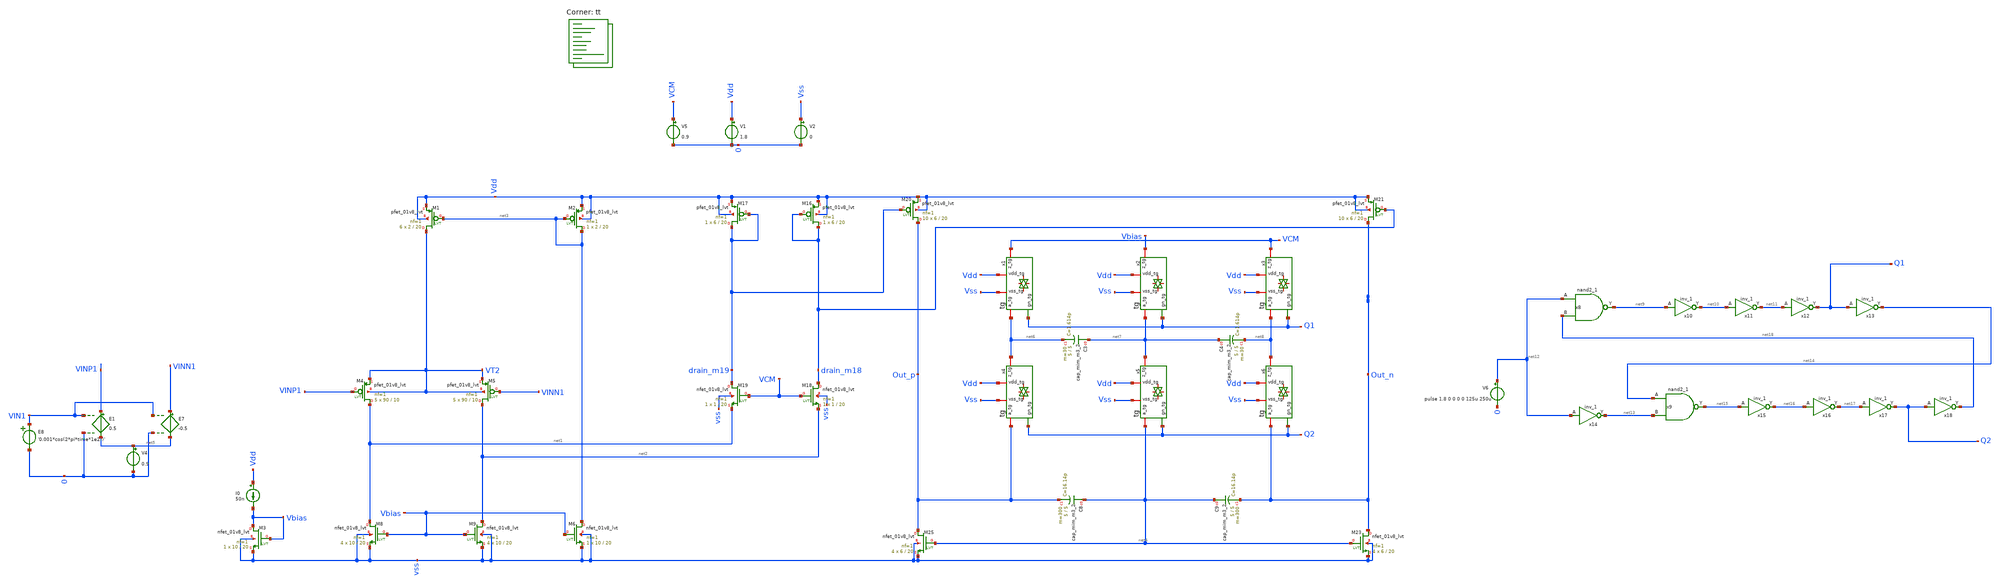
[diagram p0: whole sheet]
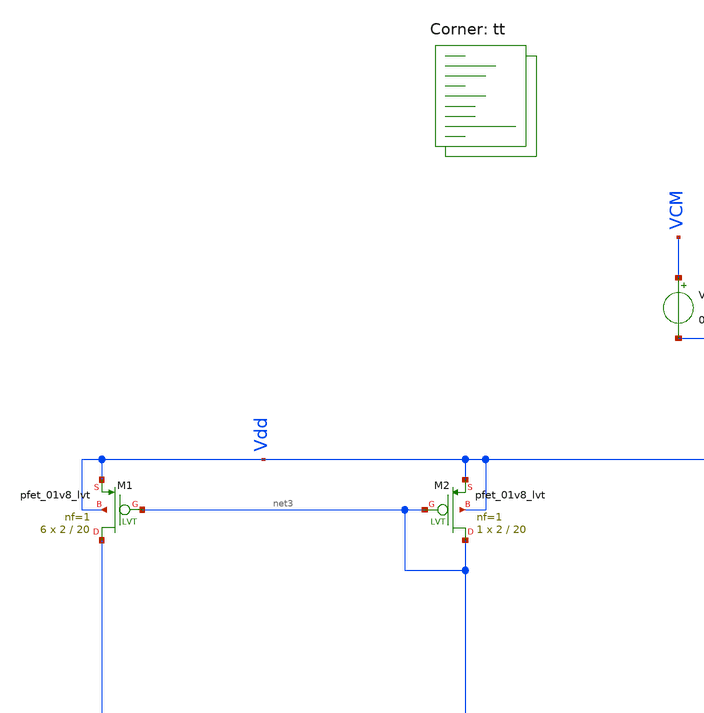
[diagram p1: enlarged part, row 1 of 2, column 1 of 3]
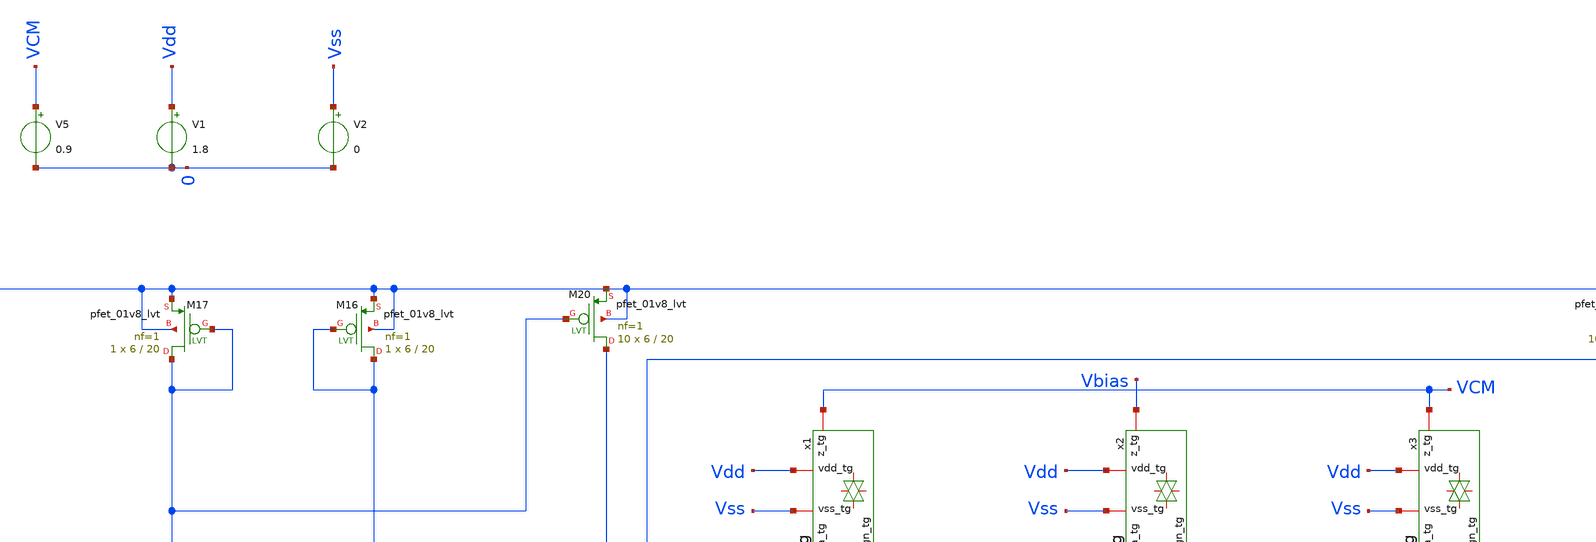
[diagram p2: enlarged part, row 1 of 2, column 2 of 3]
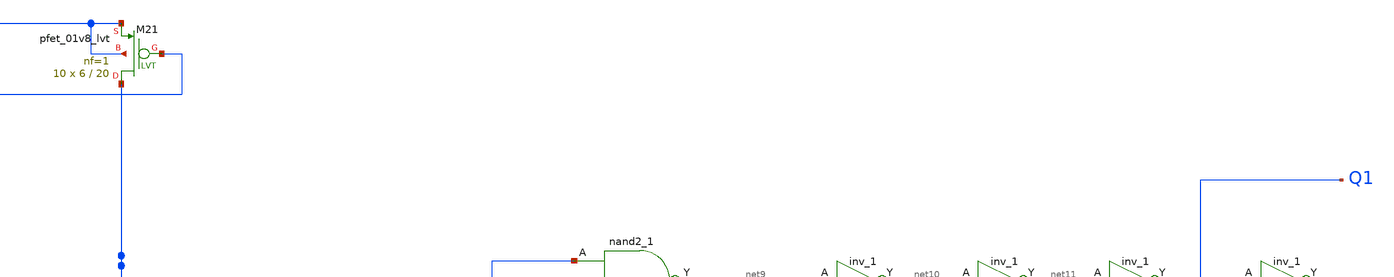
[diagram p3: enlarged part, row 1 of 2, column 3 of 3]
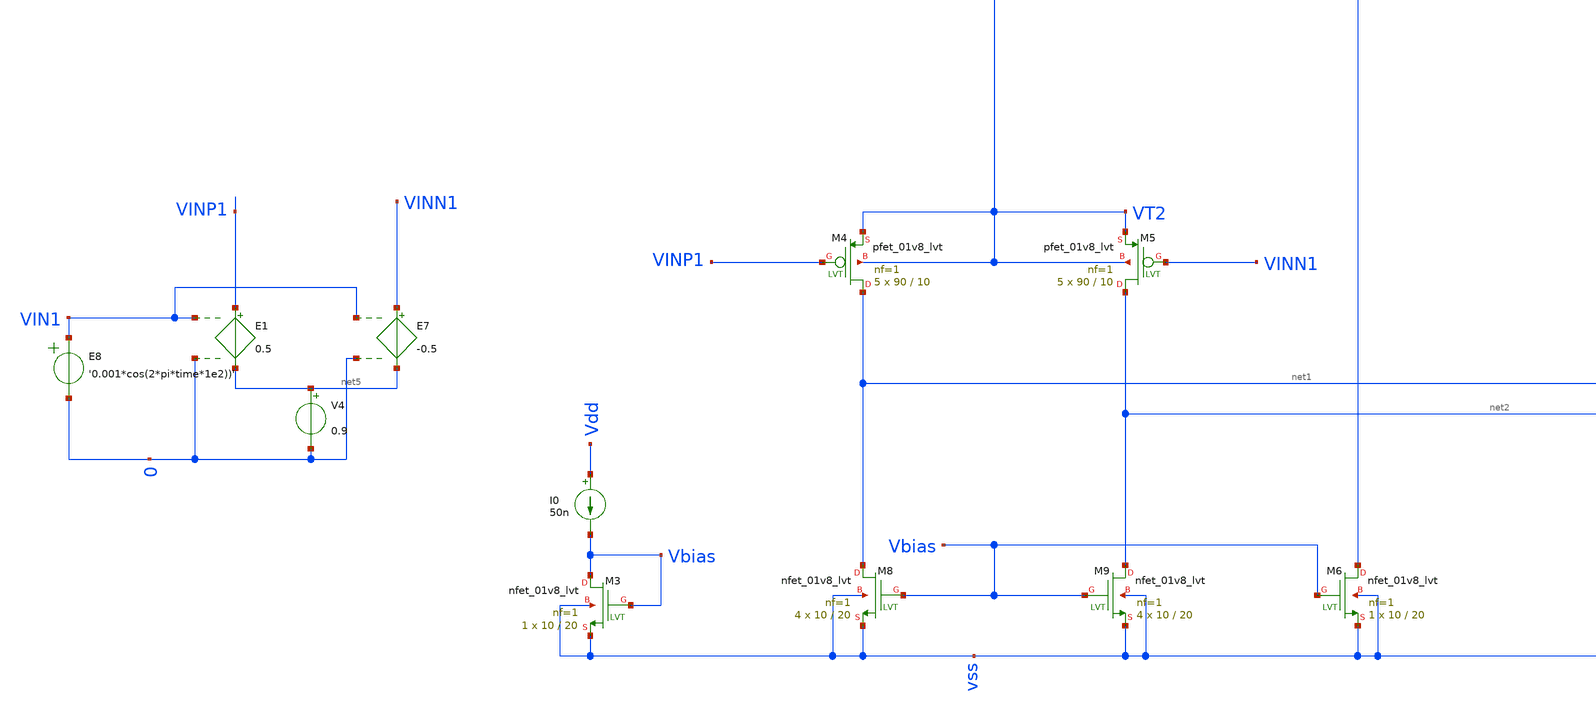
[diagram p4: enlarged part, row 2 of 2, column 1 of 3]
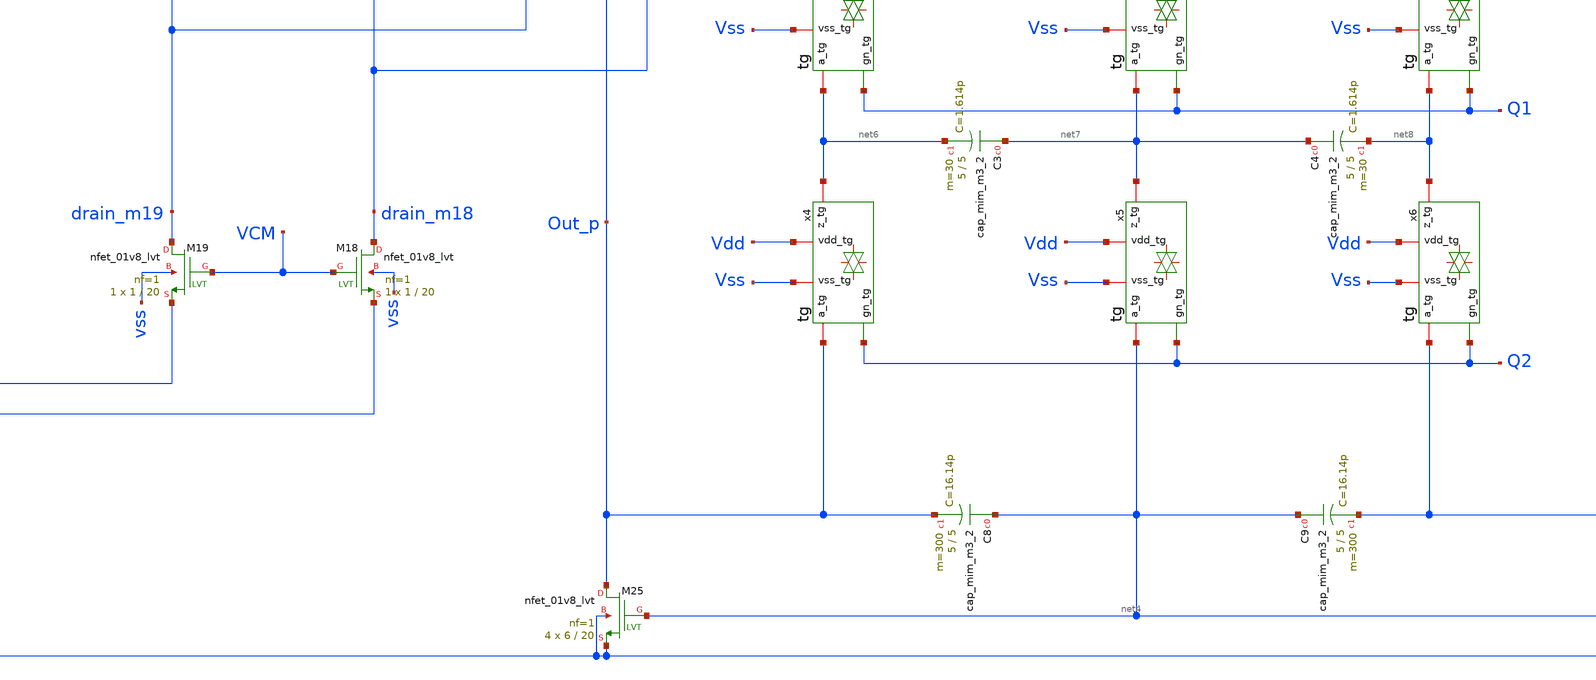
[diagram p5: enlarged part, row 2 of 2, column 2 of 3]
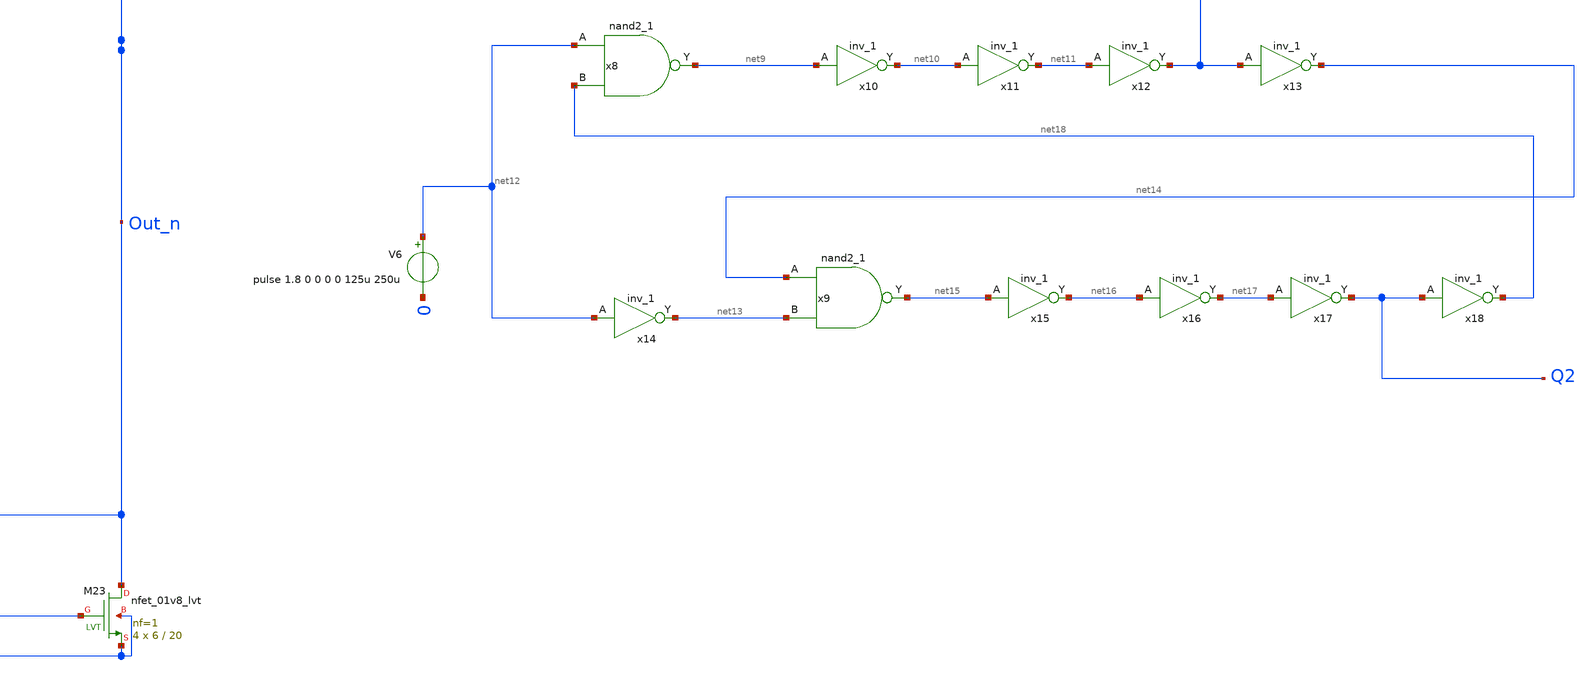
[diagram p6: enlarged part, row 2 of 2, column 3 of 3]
** sch_path: OL_transient.sch
**.subckt OL_transient
XM4 net1 VINP1 VT2 VT2 sky130_fd_pr__pfet_01v8_lvt L=10 W=90 nf=1 ad='int((nf+1)/2) * W/nf * 0.29' as='int((nf+2)/2) * W/nf * 0.29'
+ pd='2*int((nf+1)/2) * (W/nf + 0.29)' ps='2*int((nf+2)/2) * (W/nf + 0.29)' nrd='0.29 / W' nrs='0.29 / W'
+ sa=0 sb=0 sd=0 mult=5 m=5
XM5 net2 VINN1 VT2 VT2 sky130_fd_pr__pfet_01v8_lvt L=10 W=90 nf=1 ad='int((nf+1)/2) * W/nf * 0.29' as='int((nf+2)/2) * W/nf * 0.29'
+ pd='2*int((nf+1)/2) * (W/nf + 0.29)' ps='2*int((nf+2)/2) * (W/nf + 0.29)' nrd='0.29 / W' nrs='0.29 / W'
+ sa=0 sb=0 sd=0 mult=5 m=5
XM8 net1 Vbias vss vss sky130_fd_pr__nfet_01v8_lvt L=20 W=10 nf=1 ad='int((nf+1)/2) * W/nf * 0.29' as='int((nf+2)/2) * W/nf * 0.29'
+ pd='2*int((nf+1)/2) * (W/nf + 0.29)' ps='2*int((nf+2)/2) * (W/nf + 0.29)' nrd='0.29 / W' nrs='0.29 / W'
+ sa=0 sb=0 sd=0 mult=4 m=4
XM9 net2 Vbias vss vss sky130_fd_pr__nfet_01v8_lvt L=20 W=10 nf=1 ad='int((nf+1)/2) * W/nf * 0.29' as='int((nf+2)/2) * W/nf * 0.29'
+ pd='2*int((nf+1)/2) * (W/nf + 0.29)' ps='2*int((nf+2)/2) * (W/nf + 0.29)' nrd='0.29 / W' nrs='0.29 / W'
+ sa=0 sb=0 sd=0 mult=4 m=4
XM16 drain_m18 drain_m18 Vdd Vdd sky130_fd_pr__pfet_01v8_lvt L=20 W=6 nf=1 ad='int((nf+1)/2) * W/nf * 0.29'
+ as='int((nf+2)/2) * W/nf * 0.29' pd='2*int((nf+1)/2) * (W/nf + 0.29)' ps='2*int((nf+2)/2) * (W/nf + 0.29)'
+ nrd='0.29 / W' nrs='0.29 / W' sa=0 sb=0 sd=0 mult=1 m=1
XM17 drain_m19 drain_m19 Vdd Vdd sky130_fd_pr__pfet_01v8_lvt L=20 W=6 nf=1 ad='int((nf+1)/2) * W/nf * 0.29'
+ as='int((nf+2)/2) * W/nf * 0.29' pd='2*int((nf+1)/2) * (W/nf + 0.29)' ps='2*int((nf+2)/2) * (W/nf + 0.29)'
+ nrd='0.29 / W' nrs='0.29 / W' sa=0 sb=0 sd=0 mult=1 m=1
XM18 drain_m18 VCM net2 vss sky130_fd_pr__nfet_01v8_lvt L=20 W=1 nf=1 ad='int((nf+1)/2) * W/nf * 0.29'
+ as='int((nf+2)/2) * W/nf * 0.29' pd='2*int((nf+1)/2) * (W/nf + 0.29)' ps='2*int((nf+2)/2) * (W/nf + 0.29)'
+ nrd='0.29 / W' nrs='0.29 / W' sa=0 sb=0 sd=0 mult=1 m=1
XM19 drain_m19 VCM net1 vss sky130_fd_pr__nfet_01v8_lvt L=20 W=1 nf=1 ad='int((nf+1)/2) * W/nf * 0.29'
+ as='int((nf+2)/2) * W/nf * 0.29' pd='2*int((nf+1)/2) * (W/nf + 0.29)' ps='2*int((nf+2)/2) * (W/nf + 0.29)'
+ nrd='0.29 / W' nrs='0.29 / W' sa=0 sb=0 sd=0 mult=1 m=1
XM20 Out_p drain_m19 Vdd Vdd sky130_fd_pr__pfet_01v8_lvt L=20 W=6 nf=1 ad='int((nf+1)/2) * W/nf * 0.29'
+ as='int((nf+2)/2) * W/nf * 0.29' pd='2*int((nf+1)/2) * (W/nf + 0.29)' ps='2*int((nf+2)/2) * (W/nf + 0.29)'
+ nrd='0.29 / W' nrs='0.29 / W' sa=0 sb=0 sd=0 mult=10 m=10
XM21 Out_n drain_m18 Vdd Vdd sky130_fd_pr__pfet_01v8_lvt L=20 W=6 nf=1 ad='int((nf+1)/2) * W/nf * 0.29'
+ as='int((nf+2)/2) * W/nf * 0.29' pd='2*int((nf+1)/2) * (W/nf + 0.29)' ps='2*int((nf+2)/2) * (W/nf + 0.29)'
+ nrd='0.29 / W' nrs='0.29 / W' sa=0 sb=0 sd=0 mult=10 m=10
XM23 Out_n net4 vss vss sky130_fd_pr__nfet_01v8_lvt L=20 W=6 nf=1 ad='int((nf+1)/2) * W/nf * 0.29' as='int((nf+2)/2) * W/nf * 0.29'
+ pd='2*int((nf+1)/2) * (W/nf + 0.29)' ps='2*int((nf+2)/2) * (W/nf + 0.29)' nrd='0.29 / W' nrs='0.29 / W'
+ sa=0 sb=0 sd=0 mult=4 m=4
XM25 Out_p net4 vss vss sky130_fd_pr__nfet_01v8_lvt L=20 W=6 nf=1 ad='int((nf+1)/2) * W/nf * 0.29' as='int((nf+2)/2) * W/nf * 0.29'
+ pd='2*int((nf+1)/2) * (W/nf + 0.29)' ps='2*int((nf+2)/2) * (W/nf + 0.29)' nrd='0.29 / W' nrs='0.29 / W'
+ sa=0 sb=0 sd=0 mult=4 m=4
V1 Vdd 0 1.8
V2 Vss 0 0
V5 VCM 0 0.9
XM1 VT2 net3 Vdd Vdd sky130_fd_pr__pfet_01v8_lvt L=20 W=2 nf=1 ad='int((nf+1)/2) * W/nf * 0.29' as='int((nf+2)/2) * W/nf * 0.29'
+ pd='2*int((nf+1)/2) * (W/nf + 0.29)' ps='2*int((nf+2)/2) * (W/nf + 0.29)' nrd='0.29 / W' nrs='0.29 / W'
+ sa=0 sb=0 sd=0 mult=6 m=6
XM2 net3 net3 Vdd Vdd sky130_fd_pr__pfet_01v8_lvt L=20 W=2 nf=1 ad='int((nf+1)/2) * W/nf * 0.29' as='int((nf+2)/2) * W/nf * 0.29'
+ pd='2*int((nf+1)/2) * (W/nf + 0.29)' ps='2*int((nf+2)/2) * (W/nf + 0.29)' nrd='0.29 / W' nrs='0.29 / W'
+ sa=0 sb=0 sd=0 mult=1 m=1
I0 Vdd Vbias 50n
XM3 Vbias Vbias vss vss sky130_fd_pr__nfet_01v8_lvt L=20 W=10 nf=1 ad='int((nf+1)/2) * W/nf * 0.29' as='int((nf+2)/2) * W/nf * 0.29'
+ pd='2*int((nf+1)/2) * (W/nf + 0.29)' ps='2*int((nf+2)/2) * (W/nf + 0.29)' nrd='0.29 / W' nrs='0.29 / W'
+ sa=0 sb=0 sd=0 mult=1 m=1
XM6 net3 Vbias vss vss sky130_fd_pr__nfet_01v8_lvt L=20 W=10 nf=1 ad='int((nf+1)/2) * W/nf * 0.29' as='int((nf+2)/2) * W/nf * 0.29'
+ pd='2*int((nf+1)/2) * (W/nf + 0.29)' ps='2*int((nf+2)/2) * (W/nf + 0.29)' nrd='0.29 / W' nrs='0.29 / W'
+ sa=0 sb=0 sd=0 mult=1 m=1
E1 VINP1 net5 VIN1 0 0.5
E7 VINN1 net5 VIN1 0 -0.5
V4 net5 0 0.9
E8 VIN1 0 VOL=' '0.001*cos(2*pi*time*1e2))' '
XC3 net7 net6 sky130_fd_pr__cap_mim_m3_2 W=5 L=5 MF=30 m=30
XC4 net7 net8 sky130_fd_pr__cap_mim_m3_2 W=5 L=5 MF=30 m=30
XC8 net4 Out_p sky130_fd_pr__cap_mim_m3_2 W=5 L=5 MF=300 m=300
XC9 net4 Out_n sky130_fd_pr__cap_mim_m3_2 W=5 L=5 MF=300 m=300
x1 Vdd net6 VCM Vss Q1 tg
x2 Vdd net7 Vbias Vss Q1 tg
x3 Vdd net8 VCM Vss Q1 tg
x4 Vdd Out_p net6 Vss Q2 tg
x5 Vdd net4 net7 Vss Q2 tg
x6 Vdd Out_n net8 Vss Q2 tg
V6 net12 0 pulse 1.8 0 0 0 0 125u 250u
x8 net12 net18 Vss Vss Vdd Vdd net9 sky130_fd_sc_hd__nand2_1
x9 net14 net13 Vss Vss Vdd Vdd net15 sky130_fd_sc_hd__nand2_1
x10 net9 Vss Vss Vdd Vdd net10 sky130_fd_sc_hd__inv_1
x11 net10 Vss Vss Vdd Vdd net11 sky130_fd_sc_hd__inv_1
x12 net11 Vss Vss Vdd Vdd Q1 sky130_fd_sc_hd__inv_1
x13 Q1 Vss Vss Vdd Vdd net14 sky130_fd_sc_hd__inv_1
x14 net12 Vss Vss Vdd Vdd net13 sky130_fd_sc_hd__inv_1
x15 net15 Vss Vss Vdd Vdd net16 sky130_fd_sc_hd__inv_1
x16 net16 Vss Vss Vdd Vdd net17 sky130_fd_sc_hd__inv_1
x17 net17 Vss Vss Vdd Vdd Q2 sky130_fd_sc_hd__inv_1
x18 Q2 Vss Vss Vdd Vdd net18 sky130_fd_sc_hd__inv_1
**** begin user architecture code
.lib $::SKYWATER_MODELS/sky130.lib.spice tt


.options savecurrents
*ic v(VM5)=0.9 v(VM6)=0.9
.control


save all

save @m.xm11.msky130_fd_pr__pfet_01v8_lvt[id]
save @m.xm11.msky130_fd_pr__pfet_01v8_lvt[vgs]


*nmos
save @m.xm3.msky130_fd_pr__nfet_01v8_lvt[vgs]
save @m.xm3.msky130_fd_pr__nfet_01v8_lvt[vth]
save @m.xm3.msky130_fd_pr__nfet_01v8_lvt[vds]

save @m.xm6.msky130_fd_pr__nfet_01v8_lvt[vgs]
save @m.xm6.msky130_fd_pr__nfet_01v8_lvt[vth]
save @m.xm6.msky130_fd_pr__nfet_01v8_lvt[vds]

save @m.xm8.msky130_fd_pr__nfet_01v8_lvt[vgs]
save @m.xm8.msky130_fd_pr__nfet_01v8_lvt[vth]
save @m.xm8.msky130_fd_pr__nfet_01v8_lvt[vds]

save @m.xm9.msky130_fd_pr__nfet_01v8_lvt[vgs]
save @m.xm9.msky130_fd_pr__nfet_01v8_lvt[vth]
save @m.xm9.msky130_fd_pr__nfet_01v8_lvt[vds]

save @m.xm18.msky130_fd_pr__nfet_01v8_lvt[vgs]
save @m.xm18.msky130_fd_pr__nfet_01v8_lvt[vth]
save @m.xm18.msky130_fd_pr__nfet_01v8_lvt[vds]

save @m.xm19.msky130_fd_pr__nfet_01v8_lvt[vgs]
save @m.xm19.msky130_fd_pr__nfet_01v8_lvt[vth]
save @m.xm19.msky130_fd_pr__nfet_01v8_lvt[vds]

save @m.xm25.msky130_fd_pr__nfet_01v8_lvt[vgs]
save @m.xm25.msky130_fd_pr__nfet_01v8_lvt[vth]
save @m.xm25.msky130_fd_pr__nfet_01v8_lvt[vds]

*pmos

save @m.xm1.msky130_fd_pr__pfet_01v8_lvt[vgs]
save @m.xm1.msky130_fd_pr__pfet_01v8_lvt[vth]
save @m.xm1.msky130_fd_pr__pfet_01v8_lvt[vds]


save @m.xm2.msky130_fd_pr__pfet_01v8_lvt[vgs]
save @m.xm2.msky130_fd_pr__pfet_01v8_lvt[vth]
save @m.xm2.msky130_fd_pr__pfet_01v8_lvt[vds]


save @m.xm10.msky130_fd_pr__pfet_01v8_lvt[vgs]
save @m.xm10.msky130_fd_pr__pfet_01v8_lvt[vth]
save @m.xm10.msky130_fd_pr__pfet_01v8_lvt[vds]

save @m.xm13.msky130_fd_pr__pfet_01v8_lvt[vgs]
save @m.xm13.msky130_fd_pr__pfet_01v8_lvt[vth]
save @m.xm13.msky130_fd_pr__pfet_01v8_lvt[vds]

save @m.xm4.msky130_fd_pr__pfet_01v8_lvt[vgs]
save @m.xm4.msky130_fd_pr__pfet_01v8_lvt[vth]
save @m.xm4.msky130_fd_pr__pfet_01v8_lvt[vds]

save @m.xm5.msky130_fd_pr__pfet_01v8_lvt[vgs]
save @m.xm5.msky130_fd_pr__pfet_01v8_lvt[vth]
save @m.xm5.msky130_fd_pr__pfet_01v8_lvt[vds]

save @m.xm16.msky130_fd_pr__pfet_01v8_lvt[vgs]
save @m.xm16.msky130_fd_pr__pfet_01v8_lvt[vth]
save @m.xm16.msky130_fd_pr__pfet_01v8_lvt[vds]

save @m.xm17.msky130_fd_pr__pfet_01v8_lvt[vgs]
save @m.xm17.msky130_fd_pr__pfet_01v8_lvt[vth]
save @m.xm17.msky130_fd_pr__pfet_01v8_lvt[vds]

save @m.xm3.msky130_fd_pr__pfet_01v8_lvt[vgs]
save @m.xm3.msky130_fd_pr__pfet_01v8_lvt[vth]
save @m.xm3.msky130_fd_pr__pfet_01v8_lvt[vds]

save @m.xm20.msky130_fd_pr__pfet_01v8_lvt[vgs]
save @m.xm20.msky130_fd_pr__pfet_01v8_lvt[vth]
save @m.xm20.msky130_fd_pr__pfet_01v8_lvt[vds]

save @m.xm2.msky130_fd_pr__pfet_01v8_lvt[vgs]
save @m.xm2.msky130_fd_pr__pfet_01v8_lvt[vth]
save @m.xm2.msky130_fd_pr__pfet_01v8_lvt[vds]

save @m.xm21.msky130_fd_pr__pfet_01v8_lvt[vgs]
save @m.xm21.msky130_fd_pr__pfet_01v8_lvt[vth]
save @m.xm21.msky130_fd_pr__pfet_01v8_lvt[vds]

save @m.xm7.msky130_fd_pr__nfet_01v8_lvt[vth]

save @m.xm1.msky130_fd_pr__pfet_01v8[vgs]

save @m.xm1.msky130_fd_pr__nfet_01v8_lvt[gm]


save @m.xm1.msky130_fd_pr__nfet_01v8_lvt[gds]
save @m.xm2.msky130_fd_pr__pfet_01v8_lvt[gm]

save @m.xm23.msky130_fd_pr__nfet_01v8[cgs]
save @m.xm4.msky130_fd_pr__pfet_01v8[cgs]
save @m.xm2.msky130_fd_pr__pfet_01v8_lvt[cgs]



save @m.xm2.msky130_fd_pr__pfet_01v8_lvt[gds]


op
*remzerovec
write OL_transient.raw
*set appendwrite

*dc V1 0 1.8 0.01
*plot @m.xm1.msky130_fd_pr__nfet_01v8_lvt[id] @m.xm2.msky130_fd_pr__pfet_01v8_lvt[id]
*remzerovec
*write OL_transient.raw

.endc
.control
let vth=@M.XM25.msky130_fd_pr__nfet_01v8_lvt[vgs]


noise V(Out_p,Out_n) V6 dec 100 0.1 128
print inoise_total onoise_total
setplot noise1
plot inoise_spectrum




tran 10u 100m
save all
plot v(Out_p)
plot v(Out_p)-v(Out_n)
plot v(@m.xm25.msky130_fd_pr__nfet_01v8_lvt[vth]) v(@m.xm25.msky130_fd_pr__nfet_01v8_lvt[vgs])
plot
+ v(@m.xm25.msky130_fd_pr__nfet_01v8_lvt[vds])-v(@m.xm25.msky130_fd_pr__nfet_01v8_lvt[vgs])+v(@m.xm25.msky130_fd_pr__nfet_01v8_lvt[vth])

.endc






.include $::SKYWATER_STDCELLS/sky130_fd_sc_hd.spice

**** end user architecture code
**.ends

* expanding   symbol:  LNA/tg.sym # of pins=5
** sym_path: tg.sym
** sch_path: tg.sch
.subckt tg vdd_tg a_tg z_tg vss_tg gn_tg
*.iopin a_tg
*.iopin z_tg
*.ipin gn_tg
*.iopin vss_tg
*.iopin vdd_tg
XM1 a_tg gn_tg z_tg vss_tg sky130_fd_pr__nfet_01v8 L=0.2 W=1 nf=1 ad='int((nf+1)/2) * W/nf * 0.29' as='int((nf+2)/2) * W/nf * 0.29'
+ pd='2*int((nf+1)/2) * (W/nf + 0.29)' ps='2*int((nf+2)/2) * (W/nf + 0.29)' nrd='0.29 / W' nrs='0.29 / W'
+ sa=0 sb=0 sd=0 mult=1 m=1
XM2 a_tg net1 z_tg vdd_tg sky130_fd_pr__pfet_01v8 L=0.2 W=2 nf=2 ad='int((nf+1)/2) * W/nf * 0.29' as='int((nf+2)/2) * W/nf * 0.29'
+ pd='2*int((nf+1)/2) * (W/nf + 0.29)' ps='2*int((nf+2)/2) * (W/nf + 0.29)' nrd='0.29 / W' nrs='0.29 / W'
+ sa=0 sb=0 sd=0 mult=1 m=1
x10 gn_tg vss_tg vss_tg vdd_tg vdd_tg net1 sky130_fd_sc_hd__inv_1
.ends

.end
